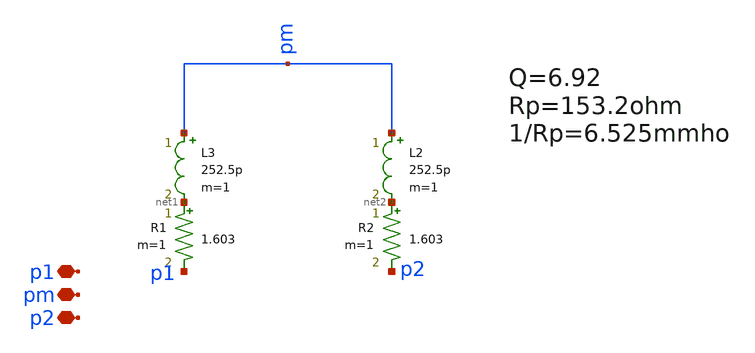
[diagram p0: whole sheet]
** sch_path: JKU_TC2/design_data/xschem/uwb_inductor.sch
**.subckt uwb_inductor p1 pm p2
*.iopin p1
*.iopin pm
*.iopin p2
L3 pm net1 252.5p m=1
R1 net1 p1 1.603 m=1
L2 pm net2 252.5p m=1
R2 net2 p2 1.603 m=1
**.ends
.end
